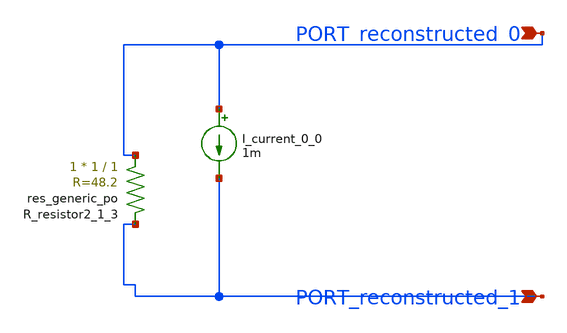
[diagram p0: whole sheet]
** sch_path: schematics/AMSNet/430.sch
**.subckt 430 PORT_reconstructed_0 PORT_reconstructed_1
*.ipin PORT_reconstructed_0
*.ipin PORT_reconstructed_1
I_current_0_0 PORT_reconstructed_0 PORT_reconstructed_1 1m
XR_resistor2_1_3 PORT_reconstructed_0 PORT_reconstructed_1 sky130_fd_pr__res_generic_po W=1 L=1 m=1
**.ends
.end
